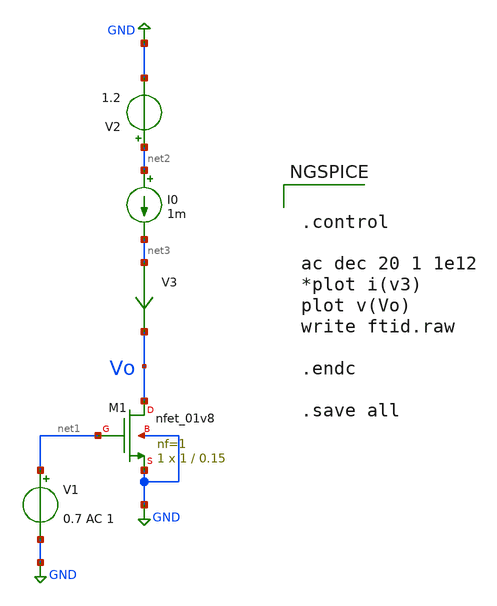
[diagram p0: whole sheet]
** sch_path: ftid.sch
**.subckt ftid
XM1 Vo net1 GND GND sky130_fd_pr__nfet_01v8 L=0.15 W=1 nf=1 ad='int((nf+1)/2) * W/nf * 0.29' as='int((nf+2)/2) * W/nf * 0.29'
+ pd='2*int((nf+1)/2) * (W/nf + 0.29)' ps='2*int((nf+2)/2) * (W/nf + 0.29)' nrd='0.29 / W' nrs='0.29 / W'
+ sa=0 sb=0 sd=0 mult=1 m=1
V1 net1 GND 0.7 AC 1
I0 net2 net3 1m
V2 net2 GND 1.2
V3 net3 Vo 0
.save i(v3)
**** begin user architecture code


.control

ac dec 20 1 1e12
*plot i(v3)
plot v(Vo)
write ftid.raw

.endc

.save all



** opencircuitdesign pdks install
.lib $::SKYWATER_MODELS/sky130.lib.spice tt


**** end user architecture code
**.ends
.GLOBAL GND
.end
